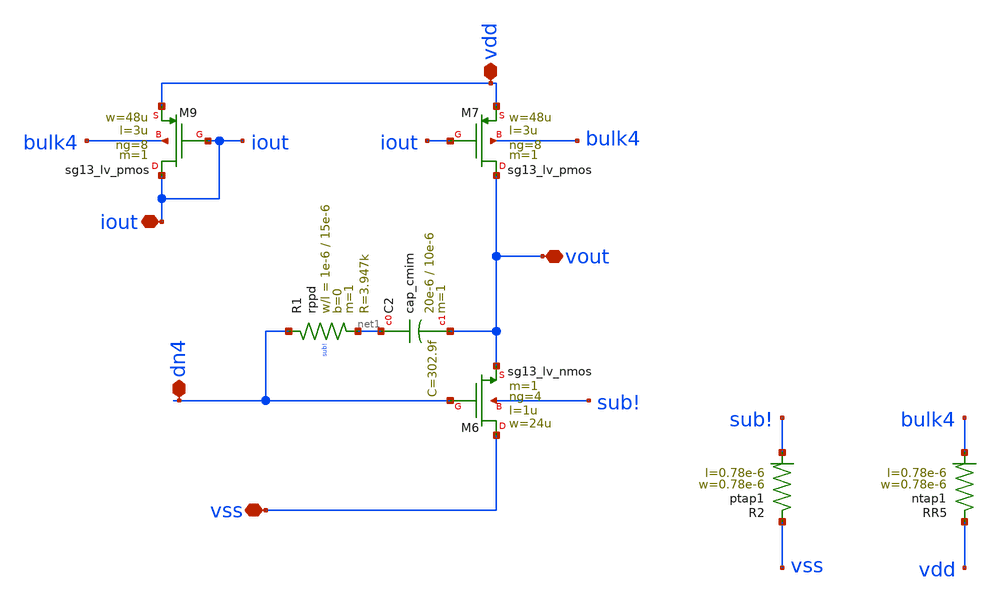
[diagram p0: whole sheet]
** sch_path: dependencies/pmu_ip/dependencies/OTA/OTA-main/schematic/xschem/output_stage.sch
**.subckt output_stage vdd iout vout vss dn4
*.iopin vdd
*.iopin iout
*.iopin vout
*.iopin vss
*.iopin dn4
XM7 vout iout vdd bulk4 sg13_lv_pmos w=48u l=3u ng=8 m=1 mm_ok=1
XM6 vss dn4 vout sub! sg13_lv_nmos w=24u l=1u ng=4 m=1 mm_ok=1
XM9 iout iout vdd bulk4 sg13_lv_pmos w=48u l=3u ng=8 m=1 mm_ok=1
XC2 net1 vout cap_cmim w=20e-6 l=10e-6 m=1 mm_ok=1
XR2 vss sub! ptap1 R=262.8 w=0.78e-6 l=0.78e-6
XR5 vdd bulk4 ntap1 R=262.8 w=0.78e-6 l=0.78e-6
XR1 dn4 net1 sub! rppd w=1e-6 l=15e-6 m=1 b=0 mm_ok=1
**.ends
.end
